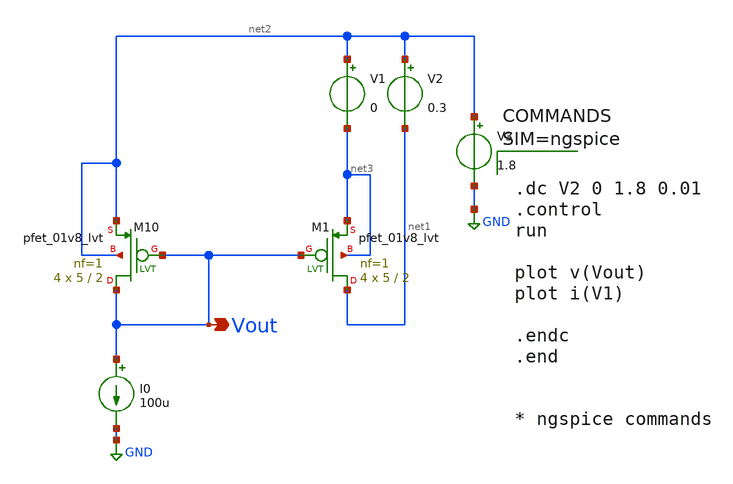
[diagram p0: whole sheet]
** sch_path: spice/cmpmos.sch
**.subckt cmpmos Vout
*.opin Vout
XM10 Vout Vout net2 net2 sky130_fd_pr__pfet_01v8_lvt L=2 W=5 nf=1 ad='int((1 + 1)/2) * 5 / 1 * 0.29'
+ as='int((1 + 2)/2) * 5 / 1 * 0.29' pd='2*int((1 + 1)/2) * (5 / 1 + 0.29)' ps='2*int((1 + 2)/2) * (5 / 1 + 0.29)'
+ nrd='0.29 / 5 ' nrs='0.29 / 5 ' sa=0 sb=0 sd=0 mult=4 m=4
XM1 net1 Vout net3 net3 sky130_fd_pr__pfet_01v8_lvt L=2 W=5 nf=1 ad='int((1 + 1)/2) * 5 / 1 * 0.29' as='int((1 + 2)/2) * 5 / 1 * 0.29'
+ pd='2*int((1 + 1)/2) * (5 / 1 + 0.29)' ps='2*int((1 + 2)/2) * (5 / 1 + 0.29)' nrd='0.29 / 5 ' nrs='0.29 / 5 '
+ sa=0 sb=0 sd=0 mult=4 m=4
I0 Vout GND 100u
V2 net2 net1 0.3
V3 net2 GND 1.8
V1 net2 net3 0
**** begin user architecture code

** opencircuitdesign pdks install
.lib $::SKYWATER_MODELS/sky130.lib.spice tt




.dc V2 0 1.8 0.01
.control
run

plot v(Vout)
plot i(V1)

.endc
.end


* ngspice commands



**** end user architecture code
**.ends
.GLOBAL GND
.end
